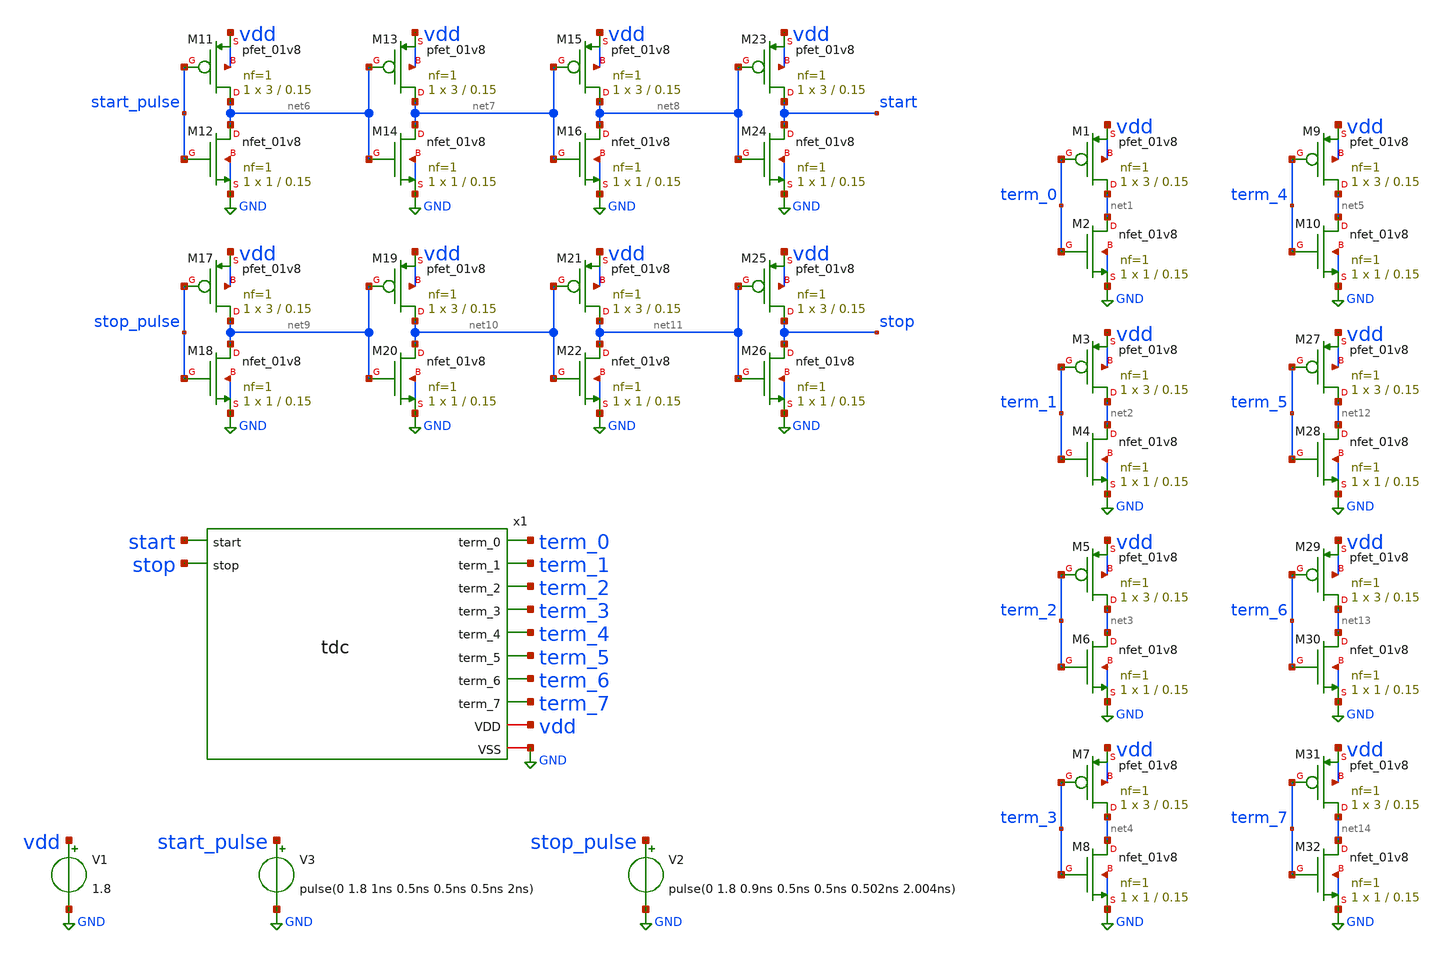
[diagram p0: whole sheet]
** sch_path: xschem/tdc_tb.sch
**.subckt tdc_tb
x1 start stop term_0 term_1 term_2 term_3 term_4 term_5 term_6 term_7 vdd GND tdc
V1 vdd GND 1.8
V2 stop_pulse GND pulse(0 1.8 0.9ns 0.5ns 0.5ns 0.502ns 2.004ns)
XM1 net1 term_0 vdd vdd sky130_fd_pr__pfet_01v8 L=0.15 W=3 nf=1 ad='int((nf+1)/2) * W/nf * 0.29' as='int((nf+2)/2) * W/nf * 0.29'
+ pd='2*int((nf+1)/2) * (W/nf + 0.29)' ps='2*int((nf+2)/2) * (W/nf + 0.29)' nrd='0.29 / W' nrs='0.29 / W'
+ sa=0 sb=0 sd=0 mult=1 m=1
XM2 net1 term_0 GND GND sky130_fd_pr__nfet_01v8 L=0.15 W=1 nf=1 ad='int((nf+1)/2) * W/nf * 0.29' as='int((nf+2)/2) * W/nf * 0.29'
+ pd='2*int((nf+1)/2) * (W/nf + 0.29)' ps='2*int((nf+2)/2) * (W/nf + 0.29)' nrd='0.29 / W' nrs='0.29 / W'
+ sa=0 sb=0 sd=0 mult=1 m=1
XM3 net2 term_1 vdd vdd sky130_fd_pr__pfet_01v8 L=0.15 W=3 nf=1 ad='int((nf+1)/2) * W/nf * 0.29' as='int((nf+2)/2) * W/nf * 0.29'
+ pd='2*int((nf+1)/2) * (W/nf + 0.29)' ps='2*int((nf+2)/2) * (W/nf + 0.29)' nrd='0.29 / W' nrs='0.29 / W'
+ sa=0 sb=0 sd=0 mult=1 m=1
XM4 net2 term_1 GND GND sky130_fd_pr__nfet_01v8 L=0.15 W=1 nf=1 ad='int((nf+1)/2) * W/nf * 0.29' as='int((nf+2)/2) * W/nf * 0.29'
+ pd='2*int((nf+1)/2) * (W/nf + 0.29)' ps='2*int((nf+2)/2) * (W/nf + 0.29)' nrd='0.29 / W' nrs='0.29 / W'
+ sa=0 sb=0 sd=0 mult=1 m=1
XM5 net3 term_2 vdd vdd sky130_fd_pr__pfet_01v8 L=0.15 W=3 nf=1 ad='int((nf+1)/2) * W/nf * 0.29' as='int((nf+2)/2) * W/nf * 0.29'
+ pd='2*int((nf+1)/2) * (W/nf + 0.29)' ps='2*int((nf+2)/2) * (W/nf + 0.29)' nrd='0.29 / W' nrs='0.29 / W'
+ sa=0 sb=0 sd=0 mult=1 m=1
XM6 net3 term_2 GND GND sky130_fd_pr__nfet_01v8 L=0.15 W=1 nf=1 ad='int((nf+1)/2) * W/nf * 0.29' as='int((nf+2)/2) * W/nf * 0.29'
+ pd='2*int((nf+1)/2) * (W/nf + 0.29)' ps='2*int((nf+2)/2) * (W/nf + 0.29)' nrd='0.29 / W' nrs='0.29 / W'
+ sa=0 sb=0 sd=0 mult=1 m=1
XM7 net4 term_3 vdd vdd sky130_fd_pr__pfet_01v8 L=0.15 W=3 nf=1 ad='int((nf+1)/2) * W/nf * 0.29' as='int((nf+2)/2) * W/nf * 0.29'
+ pd='2*int((nf+1)/2) * (W/nf + 0.29)' ps='2*int((nf+2)/2) * (W/nf + 0.29)' nrd='0.29 / W' nrs='0.29 / W'
+ sa=0 sb=0 sd=0 mult=1 m=1
XM8 net4 term_3 GND GND sky130_fd_pr__nfet_01v8 L=0.15 W=1 nf=1 ad='int((nf+1)/2) * W/nf * 0.29' as='int((nf+2)/2) * W/nf * 0.29'
+ pd='2*int((nf+1)/2) * (W/nf + 0.29)' ps='2*int((nf+2)/2) * (W/nf + 0.29)' nrd='0.29 / W' nrs='0.29 / W'
+ sa=0 sb=0 sd=0 mult=1 m=1
XM9 net5 term_4 vdd vdd sky130_fd_pr__pfet_01v8 L=0.15 W=3 nf=1 ad='int((nf+1)/2) * W/nf * 0.29' as='int((nf+2)/2) * W/nf * 0.29'
+ pd='2*int((nf+1)/2) * (W/nf + 0.29)' ps='2*int((nf+2)/2) * (W/nf + 0.29)' nrd='0.29 / W' nrs='0.29 / W'
+ sa=0 sb=0 sd=0 mult=1 m=1
XM10 net5 term_4 GND GND sky130_fd_pr__nfet_01v8 L=0.15 W=1 nf=1 ad='int((nf+1)/2) * W/nf * 0.29' as='int((nf+2)/2) * W/nf * 0.29'
+ pd='2*int((nf+1)/2) * (W/nf + 0.29)' ps='2*int((nf+2)/2) * (W/nf + 0.29)' nrd='0.29 / W' nrs='0.29 / W'
+ sa=0 sb=0 sd=0 mult=1 m=1
V3 start_pulse GND pulse(0 1.8 1ns 0.5ns 0.5ns 0.5ns 2ns)
XM11 net6 start_pulse vdd vdd sky130_fd_pr__pfet_01v8 L=0.15 W=3 nf=1 ad='int((nf+1)/2) * W/nf * 0.29'
+ as='int((nf+2)/2) * W/nf * 0.29' pd='2*int((nf+1)/2) * (W/nf + 0.29)' ps='2*int((nf+2)/2) * (W/nf + 0.29)'
+ nrd='0.29 / W' nrs='0.29 / W' sa=0 sb=0 sd=0 mult=1 m=1
XM12 net6 start_pulse GND GND sky130_fd_pr__nfet_01v8 L=0.15 W=1 nf=1 ad='int((nf+1)/2) * W/nf * 0.29'
+ as='int((nf+2)/2) * W/nf * 0.29' pd='2*int((nf+1)/2) * (W/nf + 0.29)' ps='2*int((nf+2)/2) * (W/nf + 0.29)'
+ nrd='0.29 / W' nrs='0.29 / W' sa=0 sb=0 sd=0 mult=1 m=1
XM13 net7 net6 vdd vdd sky130_fd_pr__pfet_01v8 L=0.15 W=3 nf=1 ad='int((nf+1)/2) * W/nf * 0.29' as='int((nf+2)/2) * W/nf * 0.29'
+ pd='2*int((nf+1)/2) * (W/nf + 0.29)' ps='2*int((nf+2)/2) * (W/nf + 0.29)' nrd='0.29 / W' nrs='0.29 / W'
+ sa=0 sb=0 sd=0 mult=1 m=1
XM14 net7 net6 GND GND sky130_fd_pr__nfet_01v8 L=0.15 W=1 nf=1 ad='int((nf+1)/2) * W/nf * 0.29' as='int((nf+2)/2) * W/nf * 0.29'
+ pd='2*int((nf+1)/2) * (W/nf + 0.29)' ps='2*int((nf+2)/2) * (W/nf + 0.29)' nrd='0.29 / W' nrs='0.29 / W'
+ sa=0 sb=0 sd=0 mult=1 m=1
XM15 net8 net7 vdd vdd sky130_fd_pr__pfet_01v8 L=0.15 W=3 nf=1 ad='int((nf+1)/2) * W/nf * 0.29' as='int((nf+2)/2) * W/nf * 0.29'
+ pd='2*int((nf+1)/2) * (W/nf + 0.29)' ps='2*int((nf+2)/2) * (W/nf + 0.29)' nrd='0.29 / W' nrs='0.29 / W'
+ sa=0 sb=0 sd=0 mult=1 m=1
XM16 net8 net7 GND GND sky130_fd_pr__nfet_01v8 L=0.15 W=1 nf=1 ad='int((nf+1)/2) * W/nf * 0.29' as='int((nf+2)/2) * W/nf * 0.29'
+ pd='2*int((nf+1)/2) * (W/nf + 0.29)' ps='2*int((nf+2)/2) * (W/nf + 0.29)' nrd='0.29 / W' nrs='0.29 / W'
+ sa=0 sb=0 sd=0 mult=1 m=1
XM17 net9 stop_pulse vdd vdd sky130_fd_pr__pfet_01v8 L=0.15 W=3 nf=1 ad='int((nf+1)/2) * W/nf * 0.29'
+ as='int((nf+2)/2) * W/nf * 0.29' pd='2*int((nf+1)/2) * (W/nf + 0.29)' ps='2*int((nf+2)/2) * (W/nf + 0.29)'
+ nrd='0.29 / W' nrs='0.29 / W' sa=0 sb=0 sd=0 mult=1 m=1
XM18 net9 stop_pulse GND GND sky130_fd_pr__nfet_01v8 L=0.15 W=1 nf=1 ad='int((nf+1)/2) * W/nf * 0.29'
+ as='int((nf+2)/2) * W/nf * 0.29' pd='2*int((nf+1)/2) * (W/nf + 0.29)' ps='2*int((nf+2)/2) * (W/nf + 0.29)'
+ nrd='0.29 / W' nrs='0.29 / W' sa=0 sb=0 sd=0 mult=1 m=1
XM19 net10 net9 vdd vdd sky130_fd_pr__pfet_01v8 L=0.15 W=3 nf=1 ad='int((nf+1)/2) * W/nf * 0.29' as='int((nf+2)/2) * W/nf * 0.29'
+ pd='2*int((nf+1)/2) * (W/nf + 0.29)' ps='2*int((nf+2)/2) * (W/nf + 0.29)' nrd='0.29 / W' nrs='0.29 / W'
+ sa=0 sb=0 sd=0 mult=1 m=1
XM20 net10 net9 GND GND sky130_fd_pr__nfet_01v8 L=0.15 W=1 nf=1 ad='int((nf+1)/2) * W/nf * 0.29' as='int((nf+2)/2) * W/nf * 0.29'
+ pd='2*int((nf+1)/2) * (W/nf + 0.29)' ps='2*int((nf+2)/2) * (W/nf + 0.29)' nrd='0.29 / W' nrs='0.29 / W'
+ sa=0 sb=0 sd=0 mult=1 m=1
XM21 net11 net10 vdd vdd sky130_fd_pr__pfet_01v8 L=0.15 W=3 nf=1 ad='int((nf+1)/2) * W/nf * 0.29' as='int((nf+2)/2) * W/nf * 0.29'
+ pd='2*int((nf+1)/2) * (W/nf + 0.29)' ps='2*int((nf+2)/2) * (W/nf + 0.29)' nrd='0.29 / W' nrs='0.29 / W'
+ sa=0 sb=0 sd=0 mult=1 m=1
XM22 net11 net10 GND GND sky130_fd_pr__nfet_01v8 L=0.15 W=1 nf=1 ad='int((nf+1)/2) * W/nf * 0.29' as='int((nf+2)/2) * W/nf * 0.29'
+ pd='2*int((nf+1)/2) * (W/nf + 0.29)' ps='2*int((nf+2)/2) * (W/nf + 0.29)' nrd='0.29 / W' nrs='0.29 / W'
+ sa=0 sb=0 sd=0 mult=1 m=1
XM23 start net8 vdd vdd sky130_fd_pr__pfet_01v8 L=0.15 W=3 nf=1 ad='int((nf+1)/2) * W/nf * 0.29' as='int((nf+2)/2) * W/nf * 0.29'
+ pd='2*int((nf+1)/2) * (W/nf + 0.29)' ps='2*int((nf+2)/2) * (W/nf + 0.29)' nrd='0.29 / W' nrs='0.29 / W'
+ sa=0 sb=0 sd=0 mult=1 m=1
XM24 start net8 GND GND sky130_fd_pr__nfet_01v8 L=0.15 W=1 nf=1 ad='int((nf+1)/2) * W/nf * 0.29' as='int((nf+2)/2) * W/nf * 0.29'
+ pd='2*int((nf+1)/2) * (W/nf + 0.29)' ps='2*int((nf+2)/2) * (W/nf + 0.29)' nrd='0.29 / W' nrs='0.29 / W'
+ sa=0 sb=0 sd=0 mult=1 m=1
XM25 stop net11 vdd vdd sky130_fd_pr__pfet_01v8 L=0.15 W=3 nf=1 ad='int((nf+1)/2) * W/nf * 0.29' as='int((nf+2)/2) * W/nf * 0.29'
+ pd='2*int((nf+1)/2) * (W/nf + 0.29)' ps='2*int((nf+2)/2) * (W/nf + 0.29)' nrd='0.29 / W' nrs='0.29 / W'
+ sa=0 sb=0 sd=0 mult=1 m=1
XM26 stop net11 GND GND sky130_fd_pr__nfet_01v8 L=0.15 W=1 nf=1 ad='int((nf+1)/2) * W/nf * 0.29' as='int((nf+2)/2) * W/nf * 0.29'
+ pd='2*int((nf+1)/2) * (W/nf + 0.29)' ps='2*int((nf+2)/2) * (W/nf + 0.29)' nrd='0.29 / W' nrs='0.29 / W'
+ sa=0 sb=0 sd=0 mult=1 m=1
XM27 net12 term_5 vdd vdd sky130_fd_pr__pfet_01v8 L=0.15 W=3 nf=1 ad='int((nf+1)/2) * W/nf * 0.29' as='int((nf+2)/2) * W/nf * 0.29'
+ pd='2*int((nf+1)/2) * (W/nf + 0.29)' ps='2*int((nf+2)/2) * (W/nf + 0.29)' nrd='0.29 / W' nrs='0.29 / W'
+ sa=0 sb=0 sd=0 mult=1 m=1
XM28 net12 term_5 GND GND sky130_fd_pr__nfet_01v8 L=0.15 W=1 nf=1 ad='int((nf+1)/2) * W/nf * 0.29' as='int((nf+2)/2) * W/nf * 0.29'
+ pd='2*int((nf+1)/2) * (W/nf + 0.29)' ps='2*int((nf+2)/2) * (W/nf + 0.29)' nrd='0.29 / W' nrs='0.29 / W'
+ sa=0 sb=0 sd=0 mult=1 m=1
XM29 net13 term_6 vdd vdd sky130_fd_pr__pfet_01v8 L=0.15 W=3 nf=1 ad='int((nf+1)/2) * W/nf * 0.29' as='int((nf+2)/2) * W/nf * 0.29'
+ pd='2*int((nf+1)/2) * (W/nf + 0.29)' ps='2*int((nf+2)/2) * (W/nf + 0.29)' nrd='0.29 / W' nrs='0.29 / W'
+ sa=0 sb=0 sd=0 mult=1 m=1
XM30 net13 term_6 GND GND sky130_fd_pr__nfet_01v8 L=0.15 W=1 nf=1 ad='int((nf+1)/2) * W/nf * 0.29' as='int((nf+2)/2) * W/nf * 0.29'
+ pd='2*int((nf+1)/2) * (W/nf + 0.29)' ps='2*int((nf+2)/2) * (W/nf + 0.29)' nrd='0.29 / W' nrs='0.29 / W'
+ sa=0 sb=0 sd=0 mult=1 m=1
XM31 net14 term_7 vdd vdd sky130_fd_pr__pfet_01v8 L=0.15 W=3 nf=1 ad='int((nf+1)/2) * W/nf * 0.29' as='int((nf+2)/2) * W/nf * 0.29'
+ pd='2*int((nf+1)/2) * (W/nf + 0.29)' ps='2*int((nf+2)/2) * (W/nf + 0.29)' nrd='0.29 / W' nrs='0.29 / W'
+ sa=0 sb=0 sd=0 mult=1 m=1
XM32 net14 term_7 GND GND sky130_fd_pr__nfet_01v8 L=0.15 W=1 nf=1 ad='int((nf+1)/2) * W/nf * 0.29' as='int((nf+2)/2) * W/nf * 0.29'
+ pd='2*int((nf+1)/2) * (W/nf + 0.29)' ps='2*int((nf+2)/2) * (W/nf + 0.29)' nrd='0.29 / W' nrs='0.29 / W'
+ sa=0 sb=0 sd=0 mult=1 m=1
**** begin user architecture code

** opencircuitdesign pdks install
.lib $::SKYWATER_MODELS/sky130.lib.spice tt





.tran 0.001n 200n
.save v(start) v(stop) v(term_0) v(term_1) v(term_2) v(term_3) v(term_4) v(term_5) v(term_6) v(term_7) v(x1.start_pos) v(x1.start_neg) v(x1.stop_strong) v(x1.delay_pos_0) v(x1.delay_neg_0) v(x1.delay_pos_1) v(x1.delay_neg_1) v(x1.delay_pos_2) v(x1.delay_neg_2) v(x1.delay_pos_3) v(x1.delay_neg_3) v(x1.delay_pos_4) v(x1.delay_neg_4) v(x1.delay_pos_5) v(x1.delay_neg_5) v(x1.delay_pos_6) v(x1.delay_neg_6) v(x1.delay_pos_7) v(x1.delay_neg_7)

.control
run
set wr_vecnames
wrdata tdc_tb.txt v(start) v(stop) v(term_0) v(term_1) v(term_2) v(term_3) v(term_4) v(term_5)
+ v(term_6) v(term_7) v(x1.start_pos) v(x1.start_neg) v(x1.stop_strong) v(x1.delay_pos_0) v(x1.delay_neg_0)
+ v(x1.delay_pos_1) v(x1.delay_neg_1) v(x1.delay_pos_2) v(x1.delay_neg_2) v(x1.delay_pos_3) v(x1.delay_neg_3)
+ v(x1.delay_pos_4) v(x1.delay_neg_4) v(x1.delay_pos_5) v(x1.delay_neg_5) v(x1.delay_pos_6) v(x1.delay_neg_6)
+ v(x1.delay_pos_7) v(x1.delay_neg_7)
.endc


**** end user architecture code
**.ends
.GLOBAL GND
.end
